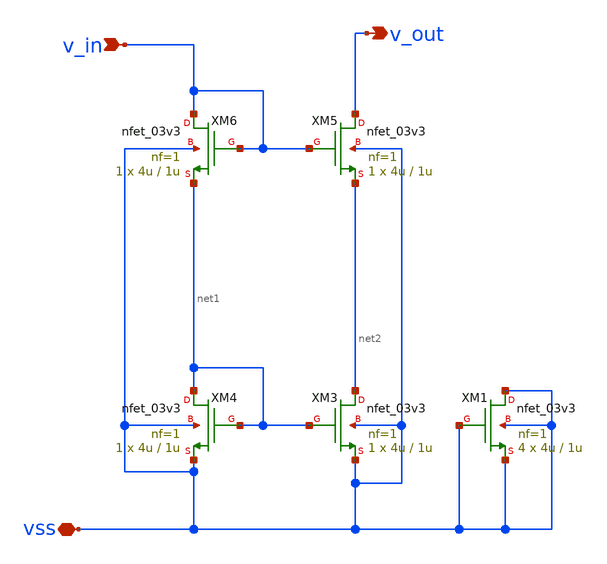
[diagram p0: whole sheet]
** sch_path: blocks/composite/regulated_cascoded_cmirror/A3_core/biased_cm/biased_cm.sch
**.subckt biased_cm v_in vss v_out
*.ipin v_in
*.iopin vss
*.opin v_out
XM3 net2 net1 vss vss nfet_03v3 L=1u W=4u nf=1 ad='int((nf+1)/2) * W/nf * 0.18u' as='int((nf+2)/2) * W/nf * 0.18u'
+ pd='2*int((nf+1)/2) * (W/nf + 0.18u)' ps='2*int((nf+2)/2) * (W/nf + 0.18u)' nrd='0.18u / W' nrs='0.18u / W'
+ sa=0 sb=0 sd=0 m=1
XM4 net1 net1 vss vss nfet_03v3 L=1u W=4u nf=1 ad='int((nf+1)/2) * W/nf * 0.18u' as='int((nf+2)/2) * W/nf * 0.18u'
+ pd='2*int((nf+1)/2) * (W/nf + 0.18u)' ps='2*int((nf+2)/2) * (W/nf + 0.18u)' nrd='0.18u / W' nrs='0.18u / W'
+ sa=0 sb=0 sd=0 m=1
XM5 v_out v_in net2 vss nfet_03v3 L=1u W=4u nf=1 ad='int((nf+1)/2) * W/nf * 0.18u' as='int((nf+2)/2) * W/nf * 0.18u'
+ pd='2*int((nf+1)/2) * (W/nf + 0.18u)' ps='2*int((nf+2)/2) * (W/nf + 0.18u)' nrd='0.18u / W' nrs='0.18u / W'
+ sa=0 sb=0 sd=0 m=1
XM6 v_in v_in net1 vss nfet_03v3 L=1u W=4u nf=1 ad='int((nf+1)/2) * W/nf * 0.18u' as='int((nf+2)/2) * W/nf * 0.18u'
+ pd='2*int((nf+1)/2) * (W/nf + 0.18u)' ps='2*int((nf+2)/2) * (W/nf + 0.18u)' nrd='0.18u / W' nrs='0.18u / W'
+ sa=0 sb=0 sd=0 m=1
XM1 vss vss vss vss nfet_03v3 L=1u W=4u nf=1 ad='int((nf+1)/2) * W/nf * 0.18u' as='int((nf+2)/2) * W/nf * 0.18u'
+ pd='2*int((nf+1)/2) * (W/nf + 0.18u)' ps='2*int((nf+2)/2) * (W/nf + 0.18u)' nrd='0.18u / W' nrs='0.18u / W'
+ sa=0 sb=0 sd=0 m=4
**.ends
.end
